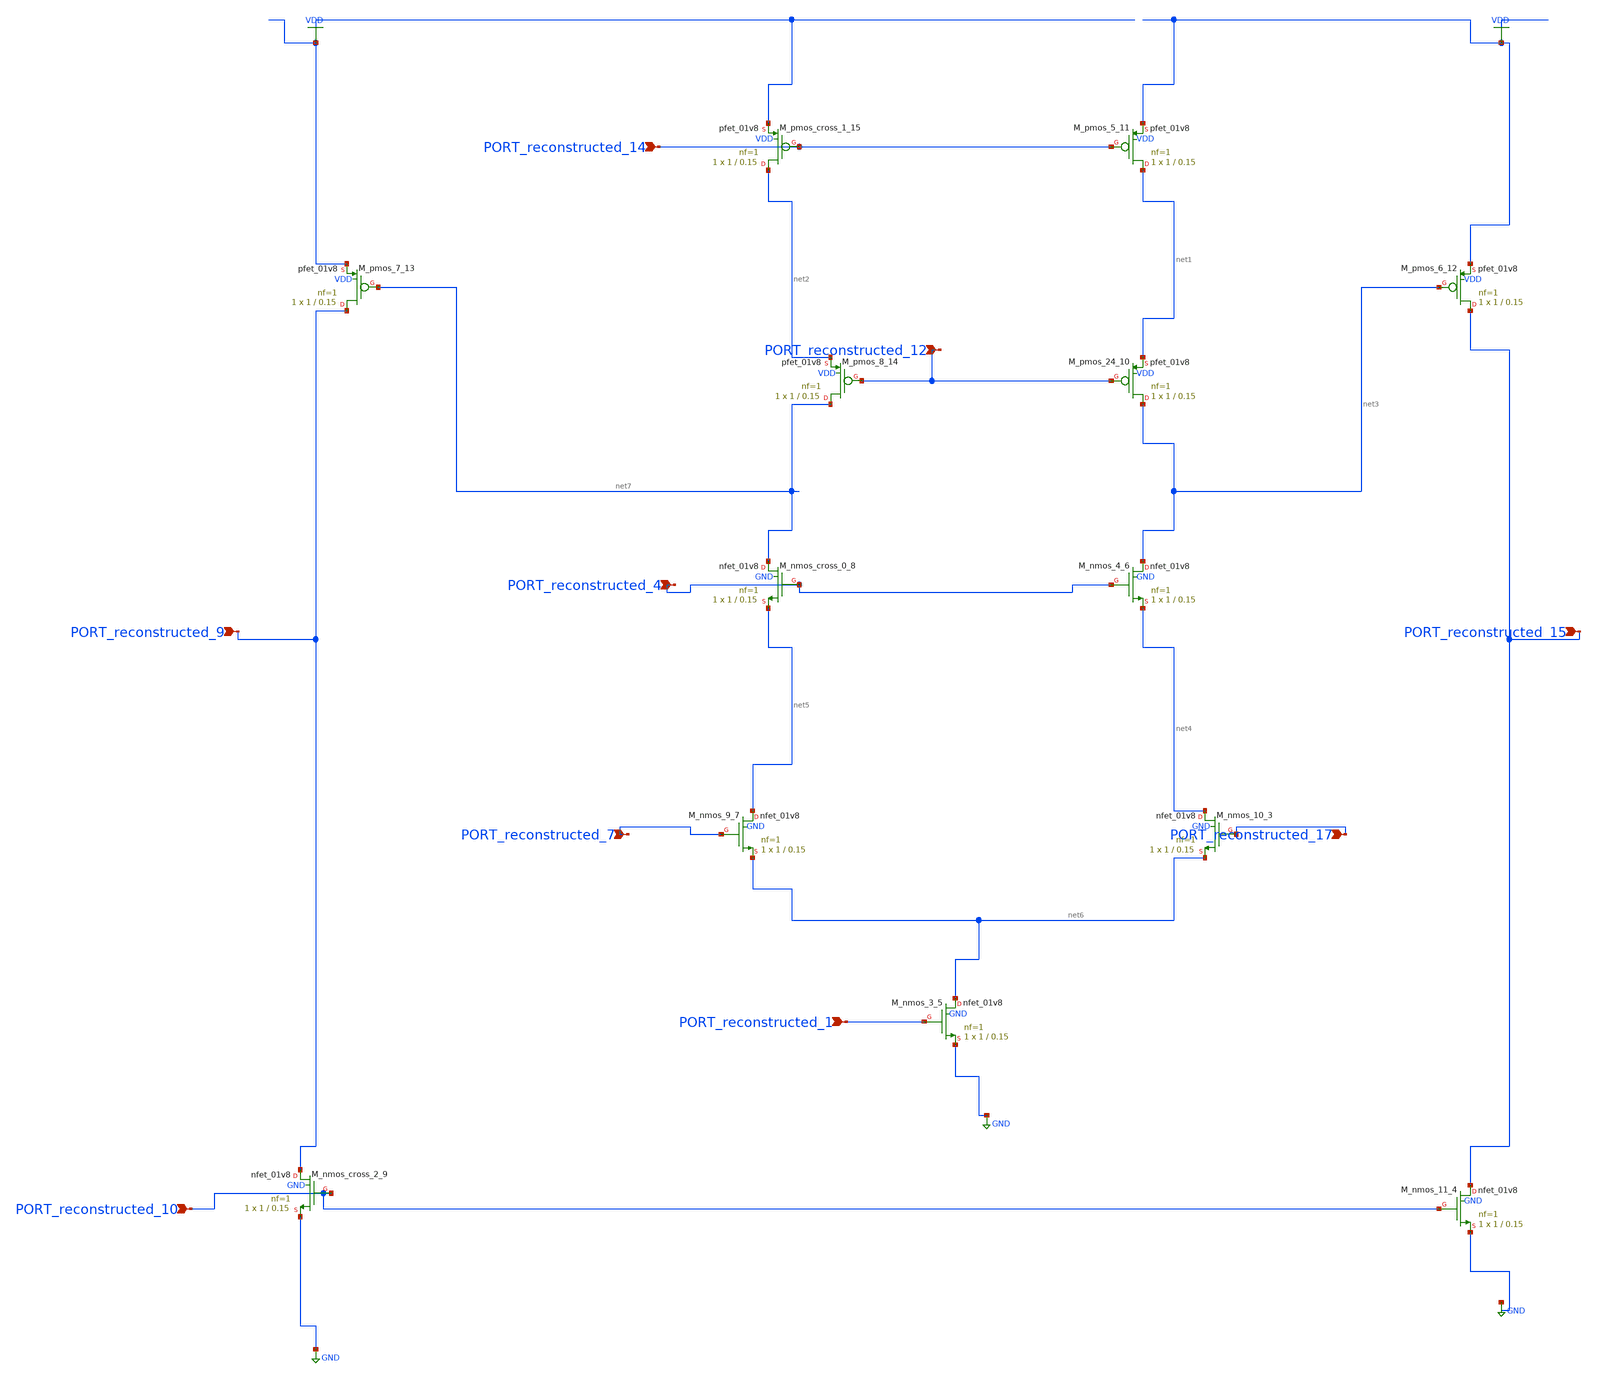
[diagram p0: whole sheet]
** sch_path: schematics/AMSNet/754.sch
**.subckt 754 PORT_reconstructed_15 PORT_reconstructed_9 PORT_reconstructed_7 PORT_reconstructed_17
*+ PORT_reconstructed_4 PORT_reconstructed_10 PORT_reconstructed_14 PORT_reconstructed_1 PORT_reconstructed_12
*.ipin PORT_reconstructed_15
*.ipin PORT_reconstructed_9
*.ipin PORT_reconstructed_7
*.ipin PORT_reconstructed_17
*.ipin PORT_reconstructed_4
*.ipin PORT_reconstructed_10
*.ipin PORT_reconstructed_14
*.ipin PORT_reconstructed_1
*.ipin PORT_reconstructed_12
XM_nmos_10_3 net4 PORT_reconstructed_17 net6 GND sky130_fd_pr__nfet_01v8 L=0.15 W=1 nf=1 ad='int((1 + 1)/2) * 1 / 1 * 0.29'
+ as='int((1 + 2)/2) * 1 / 1 * 0.29' pd='2*int((1 + 1)/2) * (1 / 1 + 0.29)' ps='2*int((1 + 2)/2) * (1 / 1 + 0.29)'
+ nrd='0.29 / 1 ' nrs='0.29 / 1 ' sa=0 sb=0 sd=0 mult=1 m=1
XM_nmos_11_4 PORT_reconstructed_15 PORT_reconstructed_10 GND GND sky130_fd_pr__nfet_01v8 L=0.15 W=1 nf=1
+ ad='int((1 + 1)/2) * 1 / 1 * 0.29' as='int((1 + 2)/2) * 1 / 1 * 0.29' pd='2*int((1 + 1)/2) * (1 / 1 + 0.29)'
+ ps='2*int((1 + 2)/2) * (1 / 1 + 0.29)' nrd='0.29 / 1 ' nrs='0.29 / 1 ' sa=0 sb=0 sd=0 mult=1 m=1
XM_nmos_3_5 net6 PORT_reconstructed_1 GND GND sky130_fd_pr__nfet_01v8 L=0.15 W=1 nf=1 ad='int((1 + 1)/2) * 1 / 1 * 0.29'
+ as='int((1 + 2)/2) * 1 / 1 * 0.29' pd='2*int((1 + 1)/2) * (1 / 1 + 0.29)' ps='2*int((1 + 2)/2) * (1 / 1 + 0.29)'
+ nrd='0.29 / 1 ' nrs='0.29 / 1 ' sa=0 sb=0 sd=0 mult=1 m=1
XM_nmos_4_6 net3 PORT_reconstructed_4 net4 GND sky130_fd_pr__nfet_01v8 L=0.15 W=1 nf=1 ad='int((1 + 1)/2) * 1 / 1 * 0.29'
+ as='int((1 + 2)/2) * 1 / 1 * 0.29' pd='2*int((1 + 1)/2) * (1 / 1 + 0.29)' ps='2*int((1 + 2)/2) * (1 / 1 + 0.29)'
+ nrd='0.29 / 1 ' nrs='0.29 / 1 ' sa=0 sb=0 sd=0 mult=1 m=1
XM_nmos_9_7 net5 PORT_reconstructed_7 net6 GND sky130_fd_pr__nfet_01v8 L=0.15 W=1 nf=1 ad='int((1 + 1)/2) * 1 / 1 * 0.29'
+ as='int((1 + 2)/2) * 1 / 1 * 0.29' pd='2*int((1 + 1)/2) * (1 / 1 + 0.29)' ps='2*int((1 + 2)/2) * (1 / 1 + 0.29)'
+ nrd='0.29 / 1 ' nrs='0.29 / 1 ' sa=0 sb=0 sd=0 mult=1 m=1
XM_nmos_cross_0_8 net7 PORT_reconstructed_4 net5 GND sky130_fd_pr__nfet_01v8 L=0.15 W=1 nf=1 ad='int((1 + 1)/2) * 1 / 1 * 0.29'
+ as='int((1 + 2)/2) * 1 / 1 * 0.29' pd='2*int((1 + 1)/2) * (1 / 1 + 0.29)' ps='2*int((1 + 2)/2) * (1 / 1 + 0.29)'
+ nrd='0.29 / 1 ' nrs='0.29 / 1 ' sa=0 sb=0 sd=0 mult=1 m=1
XM_nmos_cross_2_9 PORT_reconstructed_9 PORT_reconstructed_10 GND GND sky130_fd_pr__nfet_01v8 L=0.15 W=1
+ nf=1 ad='int((1 + 1)/2) * 1 / 1 * 0.29' as='int((1 + 2)/2) * 1 / 1 * 0.29' pd='2*int((1 + 1)/2) * (1 / 1 + 0.29)'
+ ps='2*int((1 + 2)/2) * (1 / 1 + 0.29)' nrd='0.29 / 1 ' nrs='0.29 / 1 ' sa=0 sb=0 sd=0 mult=1 m=1
XM_pmos_24_10 net3 PORT_reconstructed_12 net1 VDD sky130_fd_pr__pfet_01v8 L=0.15 W=1 nf=1 ad='int((1 + 1)/2) * 1 / 1 * 0.29'
+ as='int((1 + 2)/2) * 1 / 1 * 0.29' pd='2*int((1 + 1)/2) * (1 / 1 + 0.29)' ps='2*int((1 + 2)/2) * (1 / 1 + 0.29)'
+ nrd='0.29 / 1 ' nrs='0.29 / 1 ' sa=0 sb=0 sd=0 mult=1 m=1
XM_pmos_5_11 net1 PORT_reconstructed_14 VDD VDD sky130_fd_pr__pfet_01v8 L=0.15 W=1 nf=1 ad='int((1 + 1)/2) * 1 / 1 * 0.29'
+ as='int((1 + 2)/2) * 1 / 1 * 0.29' pd='2*int((1 + 1)/2) * (1 / 1 + 0.29)' ps='2*int((1 + 2)/2) * (1 / 1 + 0.29)'
+ nrd='0.29 / 1 ' nrs='0.29 / 1 ' sa=0 sb=0 sd=0 mult=1 m=1
XM_pmos_6_12 PORT_reconstructed_15 net3 VDD VDD sky130_fd_pr__pfet_01v8 L=0.15 W=1 nf=1 ad='int((1 + 1)/2) * 1 / 1 * 0.29'
+ as='int((1 + 2)/2) * 1 / 1 * 0.29' pd='2*int((1 + 1)/2) * (1 / 1 + 0.29)' ps='2*int((1 + 2)/2) * (1 / 1 + 0.29)'
+ nrd='0.29 / 1 ' nrs='0.29 / 1 ' sa=0 sb=0 sd=0 mult=1 m=1
XM_pmos_7_13 PORT_reconstructed_9 net7 VDD VDD sky130_fd_pr__pfet_01v8 L=0.15 W=1 nf=1 ad='int((1 + 1)/2) * 1 / 1 * 0.29'
+ as='int((1 + 2)/2) * 1 / 1 * 0.29' pd='2*int((1 + 1)/2) * (1 / 1 + 0.29)' ps='2*int((1 + 2)/2) * (1 / 1 + 0.29)'
+ nrd='0.29 / 1 ' nrs='0.29 / 1 ' sa=0 sb=0 sd=0 mult=1 m=1
XM_pmos_8_14 net7 PORT_reconstructed_12 net2 VDD sky130_fd_pr__pfet_01v8 L=0.15 W=1 nf=1 ad='int((1 + 1)/2) * 1 / 1 * 0.29'
+ as='int((1 + 2)/2) * 1 / 1 * 0.29' pd='2*int((1 + 1)/2) * (1 / 1 + 0.29)' ps='2*int((1 + 2)/2) * (1 / 1 + 0.29)'
+ nrd='0.29 / 1 ' nrs='0.29 / 1 ' sa=0 sb=0 sd=0 mult=1 m=1
XM_pmos_cross_1_15 net2 PORT_reconstructed_14 VDD VDD sky130_fd_pr__pfet_01v8 L=0.15 W=1 nf=1 ad='int((1 + 1)/2) * 1 / 1 * 0.29'
+ as='int((1 + 2)/2) * 1 / 1 * 0.29' pd='2*int((1 + 1)/2) * (1 / 1 + 0.29)' ps='2*int((1 + 2)/2) * (1 / 1 + 0.29)'
+ nrd='0.29 / 1 ' nrs='0.29 / 1 ' sa=0 sb=0 sd=0 mult=1 m=1
**.ends
.GLOBAL GND
.GLOBAL VDD
.end
